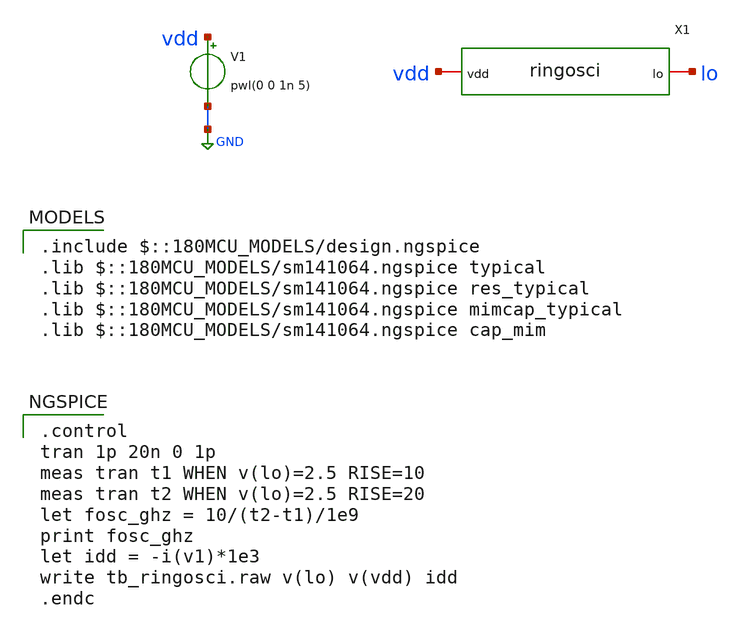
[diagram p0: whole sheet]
** sch_path: schematic pt2/sims/tb/tb_ringosci.sch
**.subckt tb_ringosci
V1 vdd GND pwl(0 0 1n 5)
X1 vdd lo ringosci
**** begin user architecture code
 .include $::180MCU_MODELS/design.ngspice
.lib $::180MCU_MODELS/sm141064.ngspice typical
.lib $::180MCU_MODELS/sm141064.ngspice res_typical
.lib $::180MCU_MODELS/sm141064.ngspice mimcap_typical
.lib $::180MCU_MODELS/sm141064.ngspice cap_mim

.control
tran 1p 20n 0 1p
meas tran t1 WHEN v(lo)=2.5 RISE=10
meas tran t2 WHEN v(lo)=2.5 RISE=20
let fosc_ghz = 10/(t2-t1)/1e9
print fosc_ghz
let idd = -i(v1)*1e3
write tb_ringosci.raw v(lo) v(vdd) idd
.endc

**** end user architecture code
**.ends
.GLOBAL GND
.end
